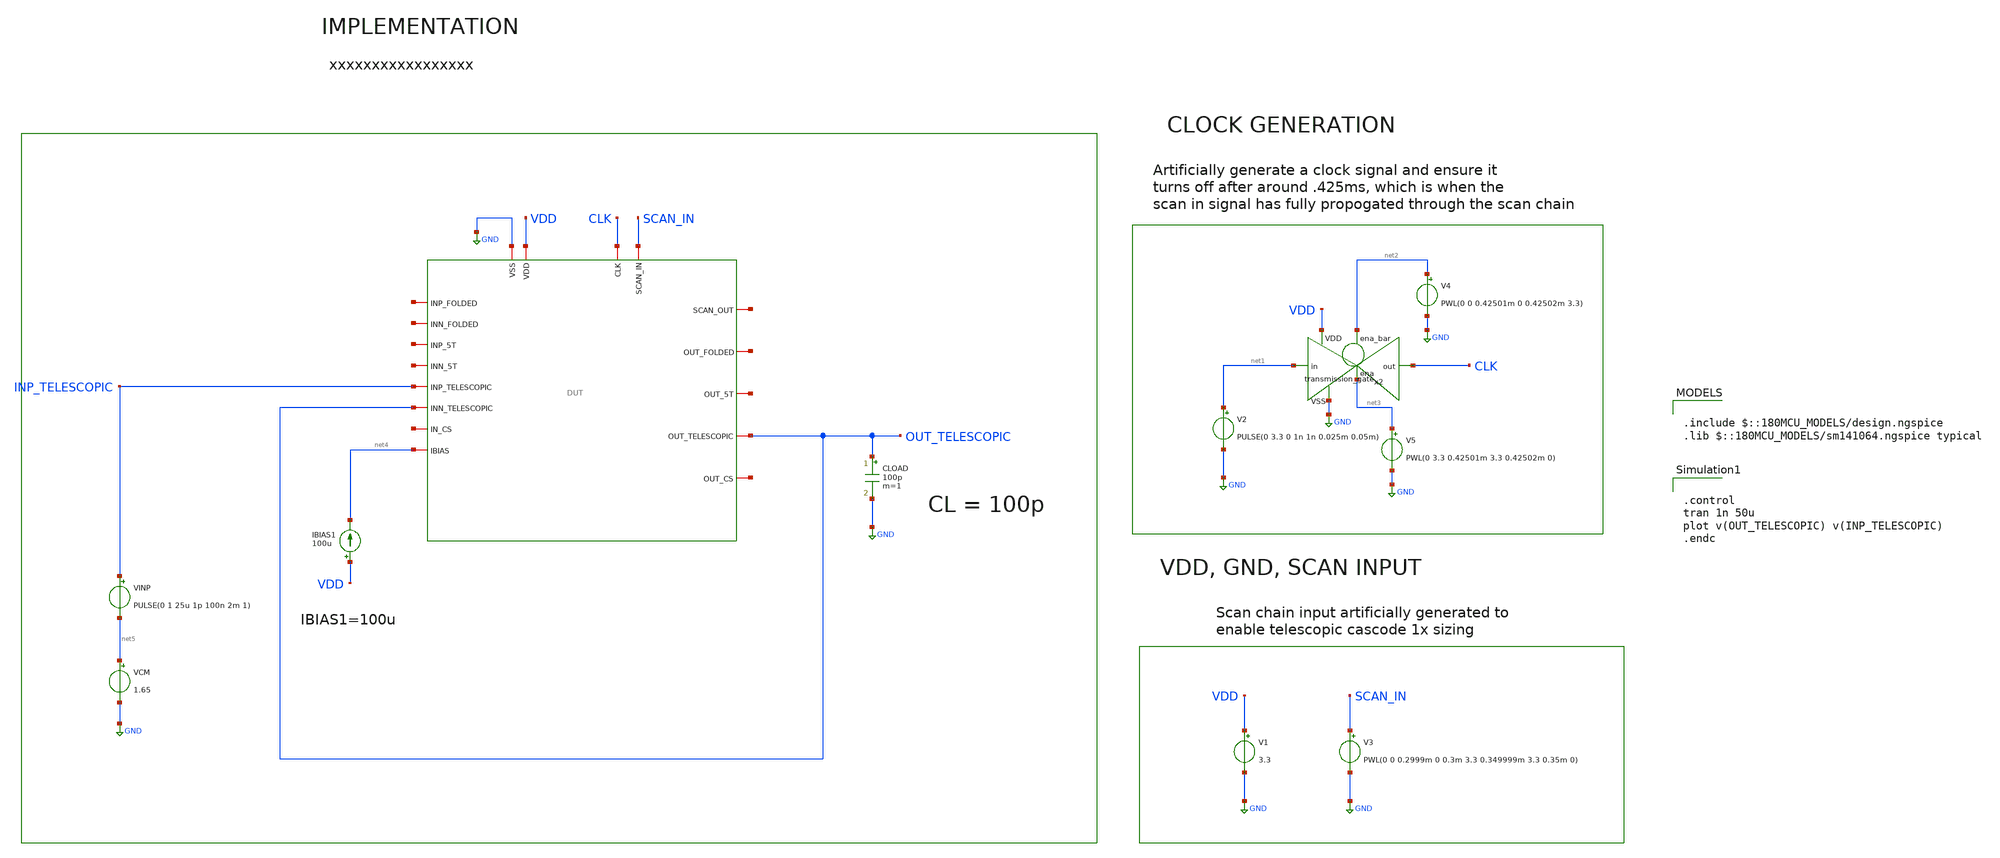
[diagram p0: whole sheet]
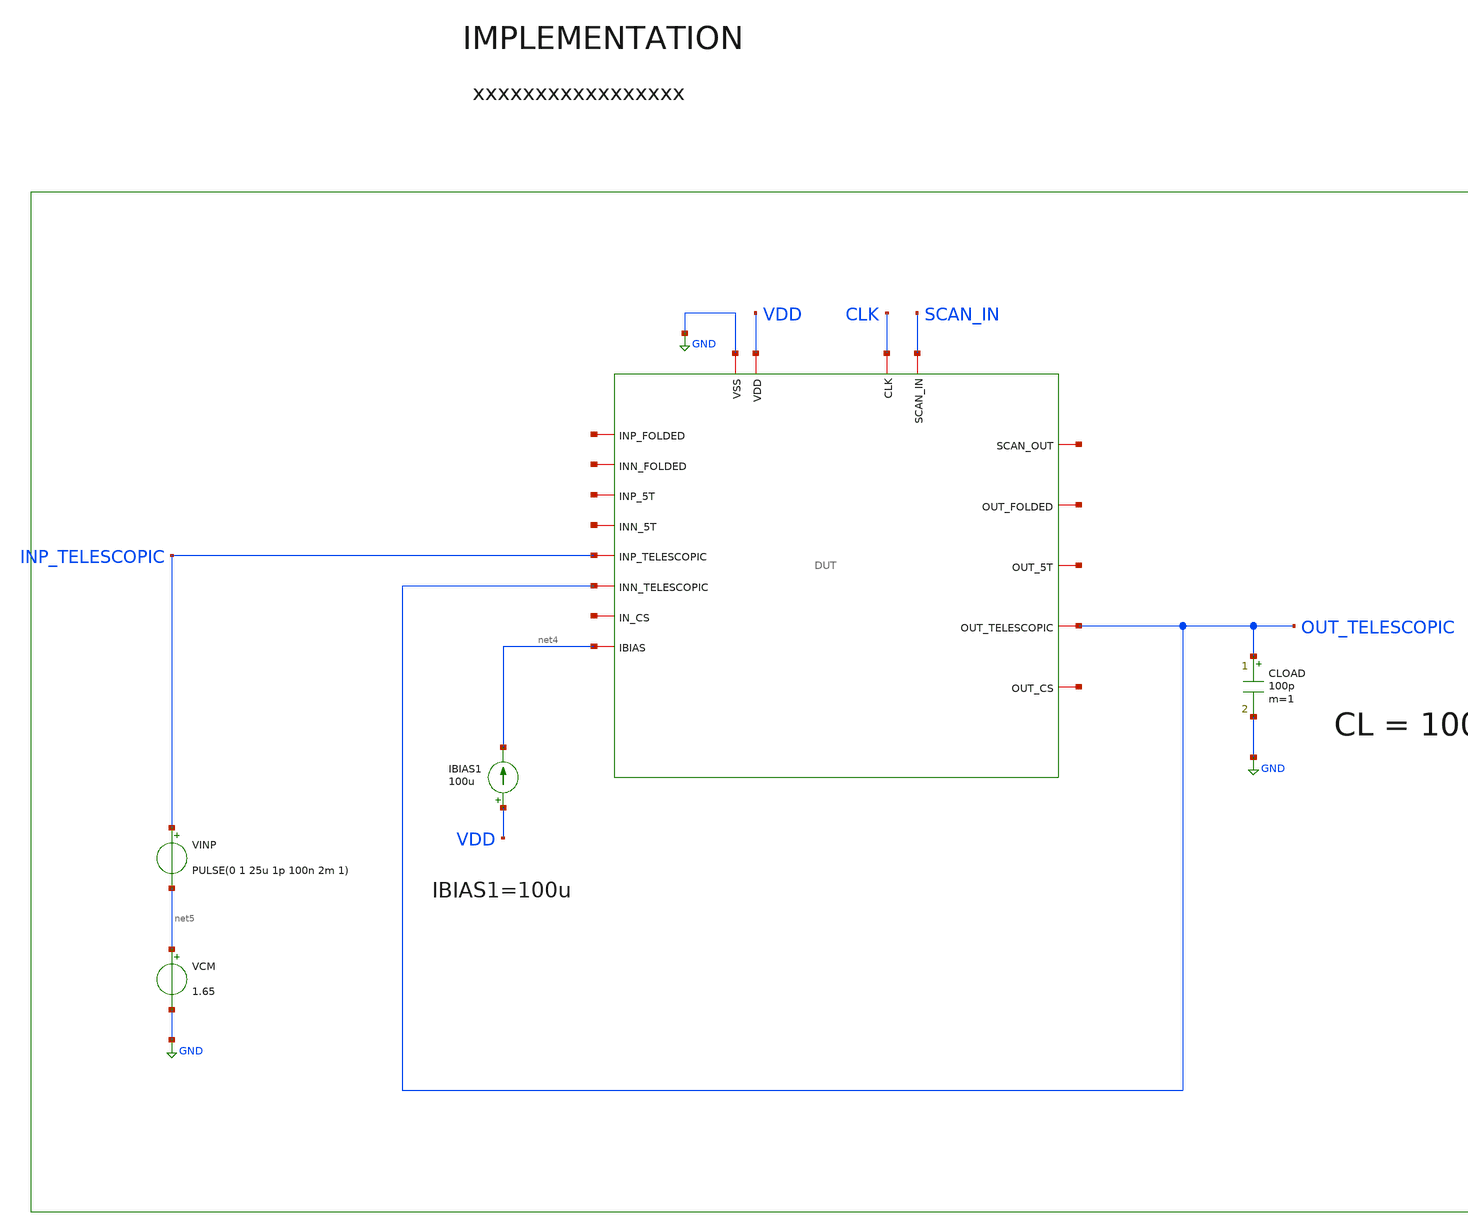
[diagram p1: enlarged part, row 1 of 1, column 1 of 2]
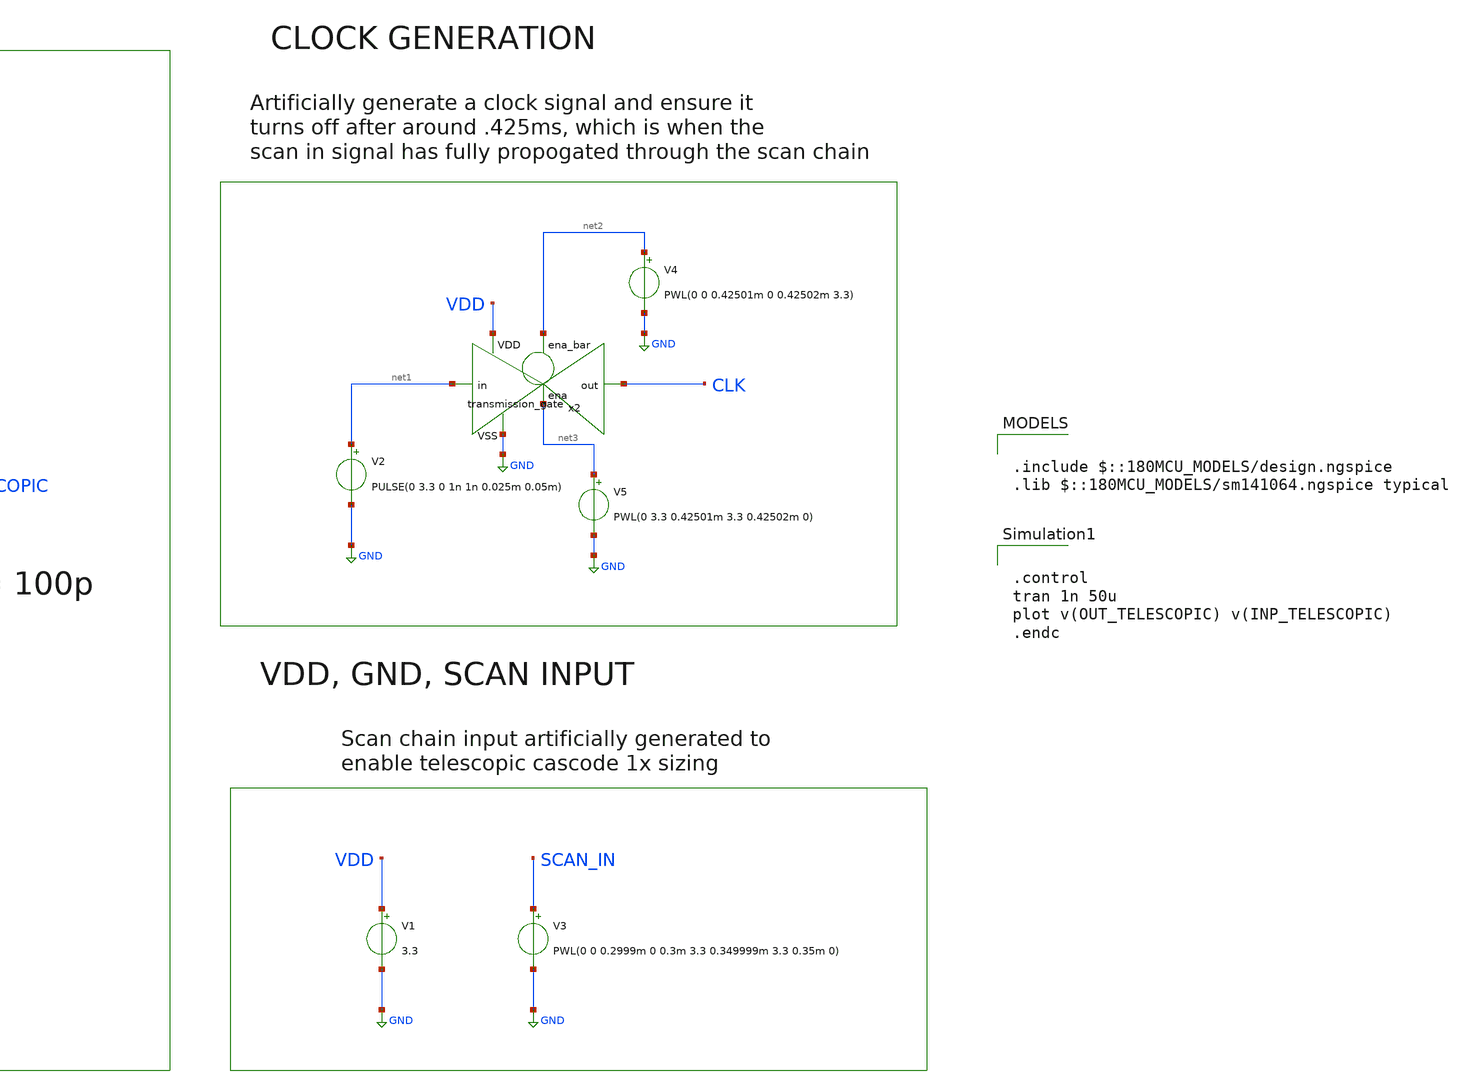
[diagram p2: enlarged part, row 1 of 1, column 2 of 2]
** sch_path: designs/libs/core_tb/mpg/ota_telescopic/unity_gain_step.sch
**.subckt unity_gain_step
V3 SCAN_IN GND PWL(0 0 0.2999m 0 0.3m 3.3 0.349999m 3.3 0.35m 0)
V1 VDD GND 3.3
V2 net1 GND PULSE(0 3.3 0 1n 1n 0.025m 0.05m)
x2 net2 VDD CLK net1 GND net3 transmission_gate
V4 net2 GND PWL(0 0 0.42501m 0 0.42502m 3.3)
V5 net3 GND PWL(0 3.3 0.42501m 3.3 0.42502m 0)
IBIAS1 VDD net4 100u
CLOAD OUT_TELESCOPIC GND 100p m=1
x1 CLK net6 SCAN_IN GND VDD net7 net8 net9 net4 net10 net11 net12 INP_TELESCOPIC OUT_TELESCOPIC
+ net13 net14 OUT_TELESCOPIC DUT
VINP INP_TELESCOPIC net5 PULSE(0 1 25u 1p 100n 2m 1)
VCM net5 GND 1.65
**** begin user architecture code

.include $::180MCU_MODELS/design.ngspice
.lib $::180MCU_MODELS/sm141064.ngspice typical



.control
tran 1n 50u
plot v(OUT_TELESCOPIC) v(INP_TELESCOPIC)
.endc


**** end user architecture code
**.ends
.GLOBAL GND
.end
